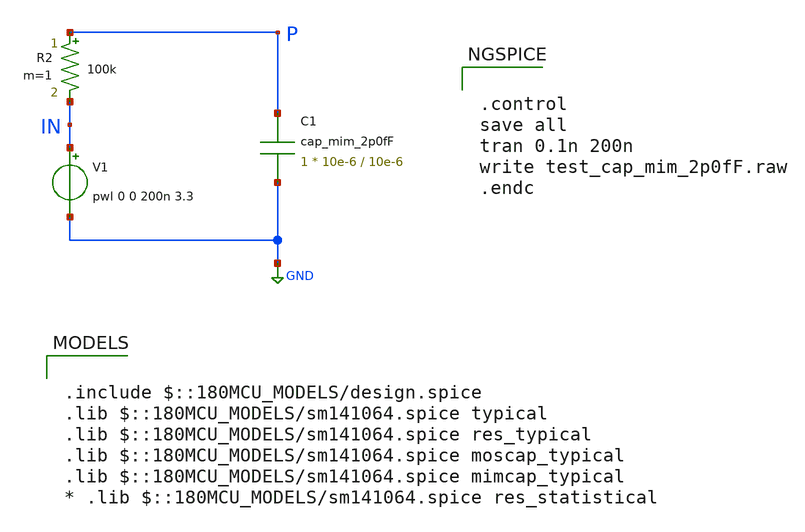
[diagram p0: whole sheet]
** sch_path: cells/xschem/tests/test_cap_mim_2p0fF.sch
* Copyright 2022 GlobalFoundries PDK Authors
* Licensed under the Apache License, Version 2.0 (the "License");
* you may not use this file except in compliance with the License.
* You may obtain a copy of the License at
* https://www.apache.org/licenses/LICENSE-2.0
* Unless required by applicable law or agreed to in writing, software
* distributed under the License is distributed on an "AS IS" BASIS,
* WITHOUT WARRANTIES OR CONDITIONS OF ANY KIND, either express or implied.
* See the License for the specific language governing permissions and
* limitations under the License.
**.subckt test_cap_mim_2p0fF
XC1 P GND cap_mim_2p0fF c_width=10e-6 c_length=10e-6 m=1
V1 IN GND pwl 0 0 200n 3.3
R2 P IN 100k m=1
**** begin user architecture code

.include $::180MCU_MODELS/design.spice
.lib $::180MCU_MODELS/sm141064.spice typical
.lib $::180MCU_MODELS/sm141064.spice res_typical
.lib $::180MCU_MODELS/sm141064.spice moscap_typical
.lib $::180MCU_MODELS/sm141064.spice mimcap_typical
* .lib $::180MCU_MODELS/sm141064.spice res_statistical



.control
save all
tran 0.1n 200n
write test_cap_mim_2p0fF.raw
.endc


**** end user architecture code
**.ends
.GLOBAL GND
.end
